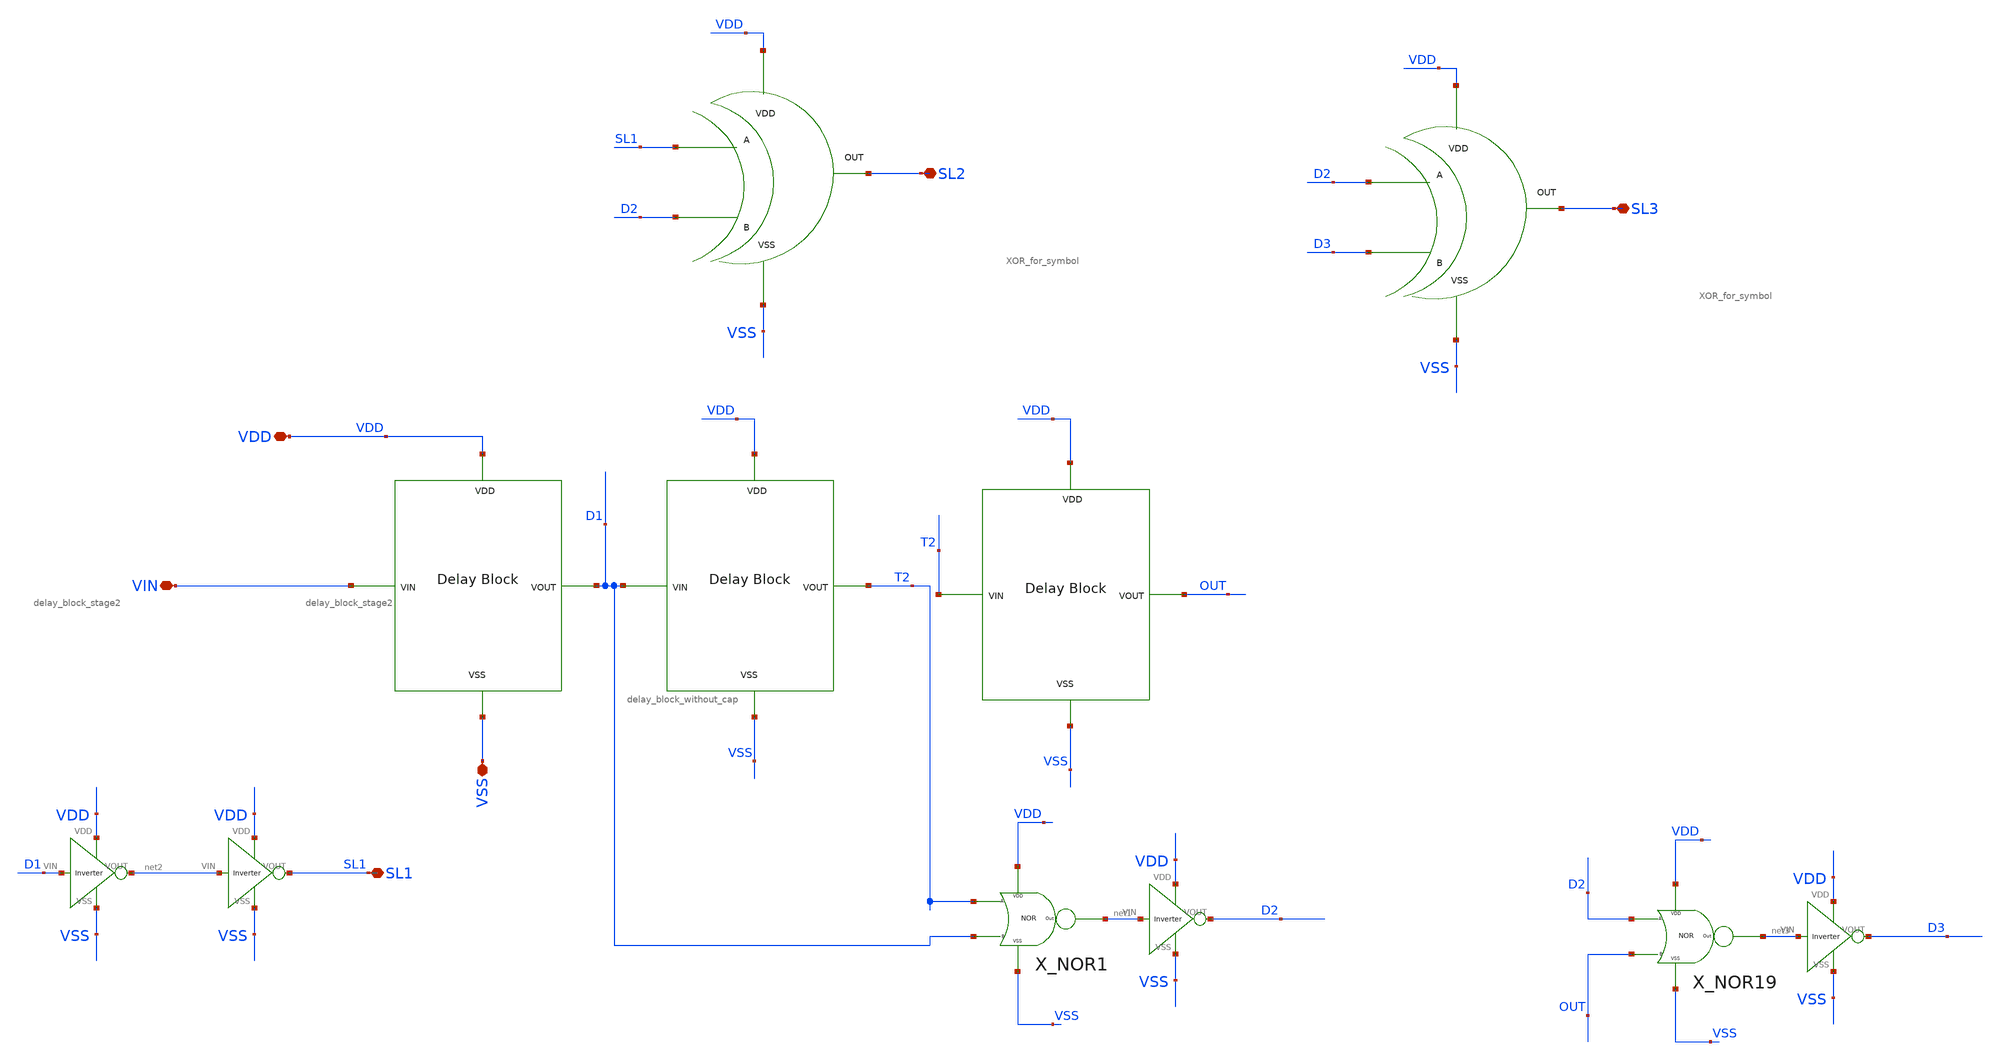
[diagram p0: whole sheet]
** sch_path: xschem/DC_DC_Converter_xschem/OTHERS/DC_DC_Converter_JV10/Delay_block_revised/Delay_block_final_symbol.sch
**.subckt Delay_block_final_symbol SL1 SL2 SL3 VDD VIN VSS
*.iopin SL1
*.iopin SL2
*.iopin SL3
*.iopin VDD
*.iopin VIN
*.iopin VSS
x1 D1 VIN VDD VSS delay_block_stage2
x2 T2 D1 VDD VSS delay_block_stage2
x4 VDD VSS SL1 D2 SL2 XOR_for_symbol
x5 VDD VSS D2 D3 SL3 XOR_for_symbol
x3 OUT T2 VDD VSS delay_block_without_cap
X_NOR19 VDD VSS D2 OUT net3 NOR
X_NOR1 VDD VSS T2 D1 net1 NOR
X3 VSS VDD D1 net2 Inverter
X2 VSS VDD net2 SL1 Inverter
X1 VSS VDD net1 D2 Inverter
X4 VSS VDD net3 D3 Inverter
**.ends
.end
